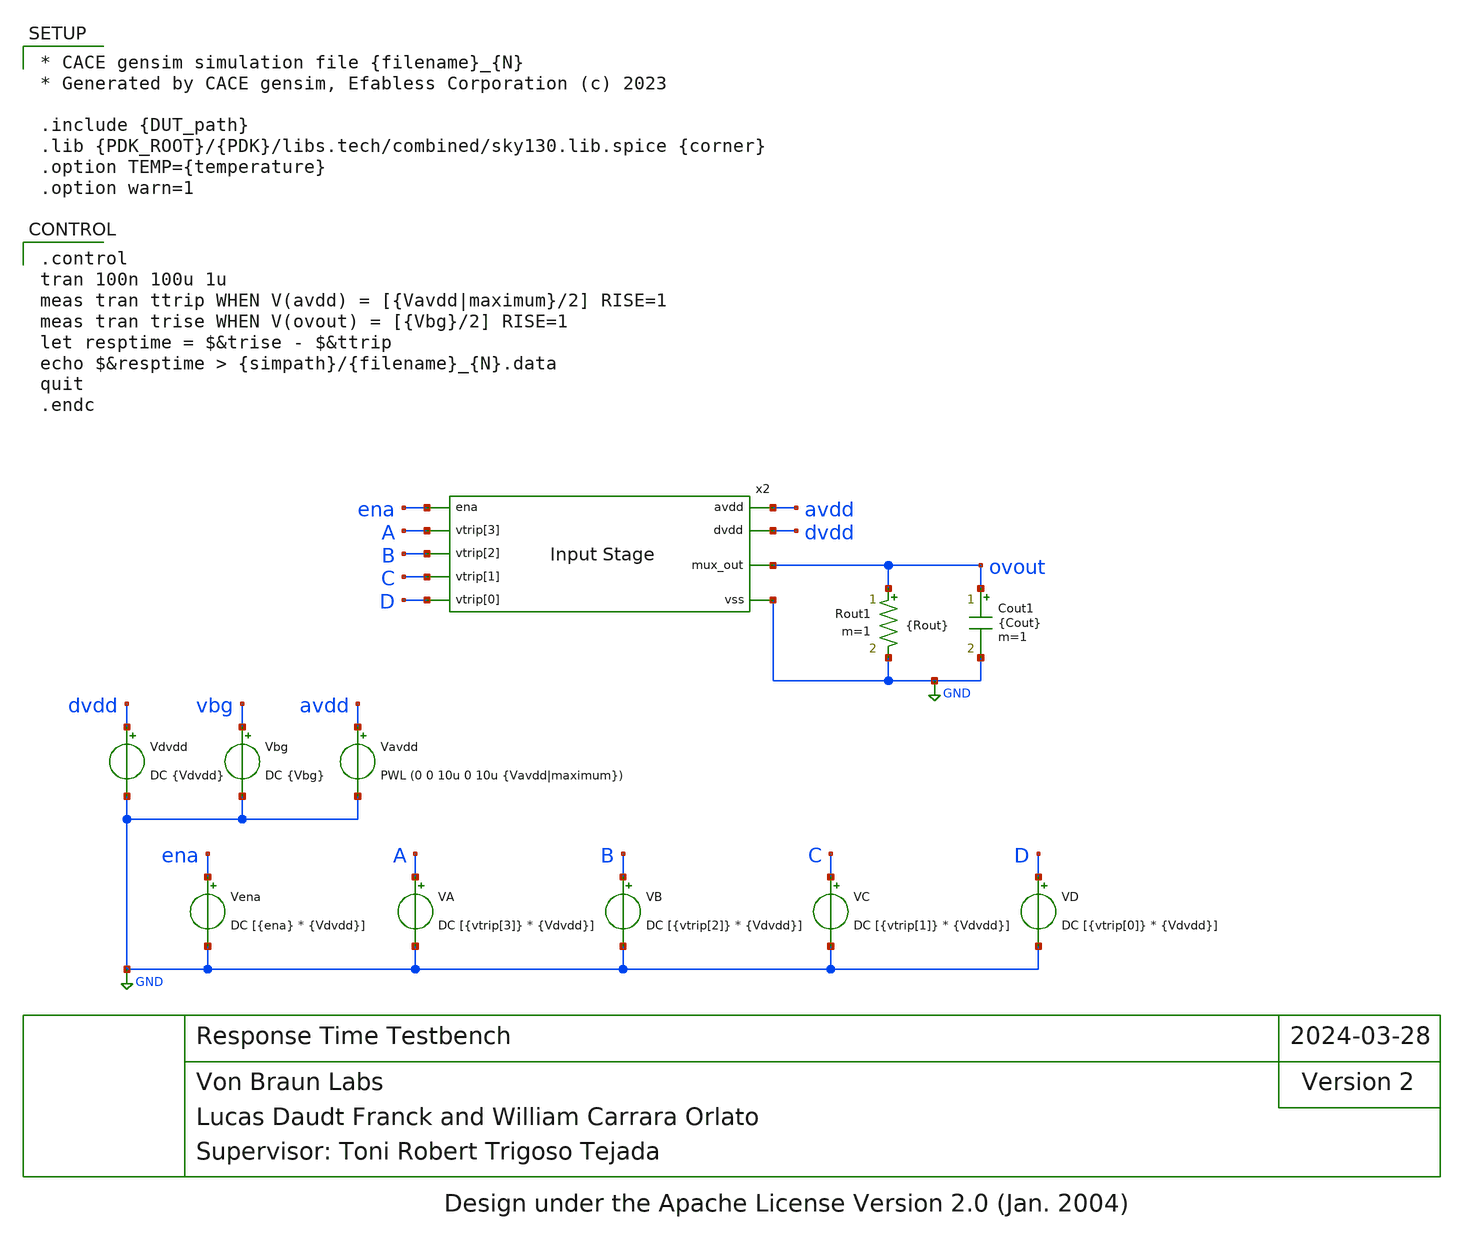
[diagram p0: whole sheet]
** sch_path: blocks/input/cace/tb_resptime.sch
* Design under the Apache License Version 2.0 (Jan. 2004)
**.subckt tb_resptime
Vavdd avdd GND PWL (0 0 10u 0 10u {Vavdd|maximum})
Vdvdd dvdd GND DC {Vdvdd}
Vbg vbg GND DC {Vbg}
Vena ena GND DC [{ena} * {Vdvdd}]
VA A GND DC [{vtrip[3]} * {Vdvdd}]
VB B GND DC [{vtrip[2]} * {Vdvdd}]
VC C GND DC [{vtrip[1]} * {Vdvdd}]
VD D GND DC [{vtrip[0]} * {Vdvdd}]
Cout1 ovout GND {Cout} m=1
Rout1 ovout GND {Rout} m=1
x2 avdd dvdd ena A GND B ovout C D input
**** begin user architecture code

* CACE gensim simulation file {filename}_{N}
* Generated by CACE gensim, Efabless Corporation (c) 2023

.include {DUT_path}
.lib {PDK_ROOT}/{PDK}/libs.tech/combined/sky130.lib.spice {corner}
.option TEMP={temperature}
.option warn=1



.control
tran 100n 100u 1u
meas tran ttrip WHEN V(avdd) = [{Vavdd|maximum}/2] RISE=1
meas tran trise WHEN V(ovout) = [{Vbg}/2] RISE=1
let resptime = $&trise - $&ttrip
echo $&resptime > {simpath}/{filename}_{N}.data
quit
.endc


**** end user architecture code
**.ends
.GLOBAL GND
.end
